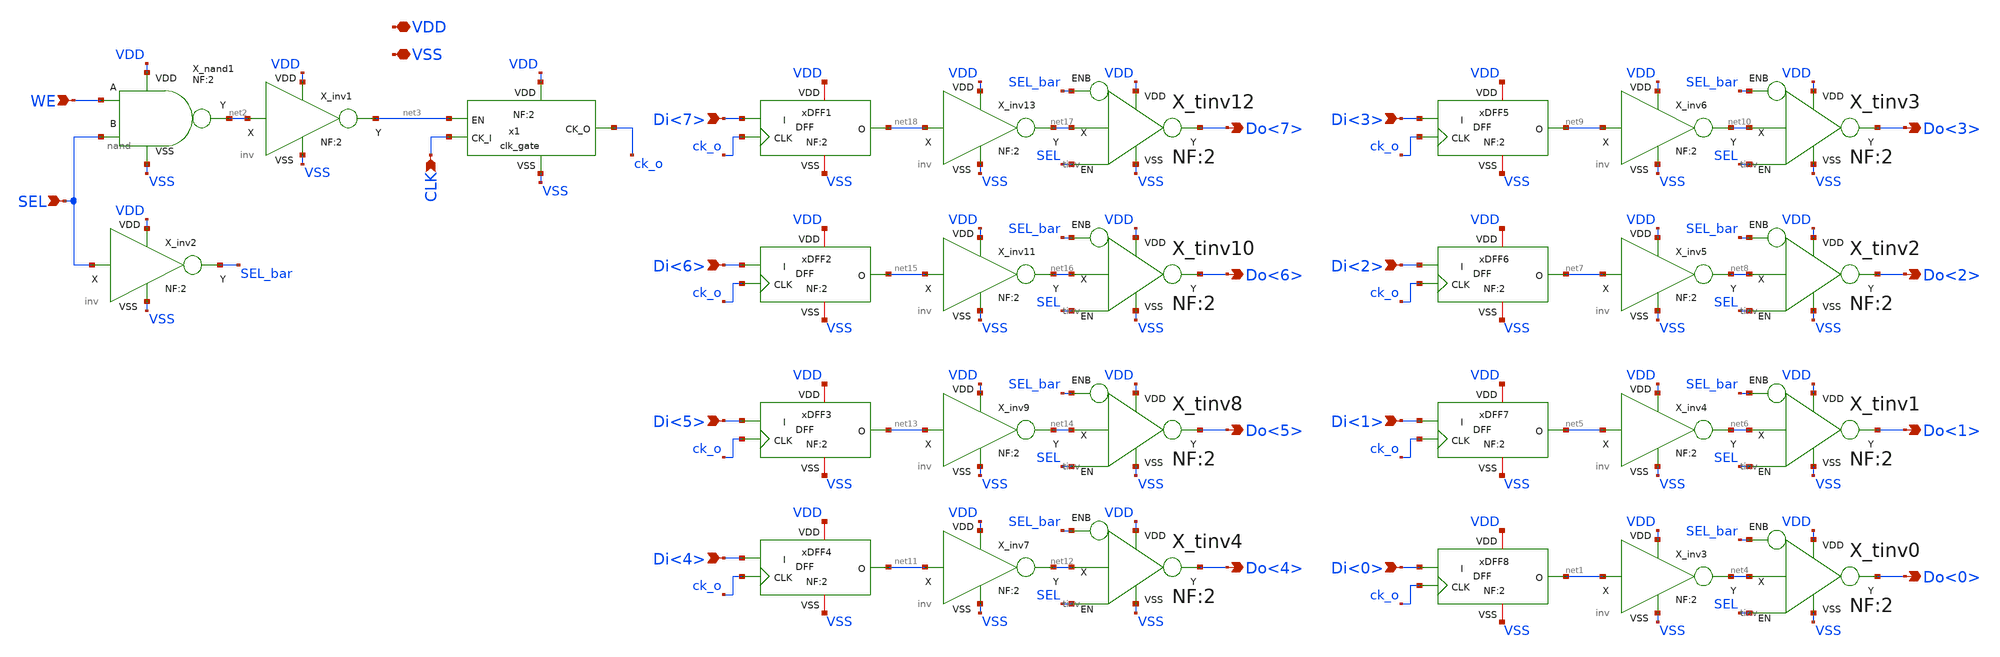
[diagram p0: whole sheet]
** sch_path: xschem_lib/sylee21/byte_dff.sch
**.subckt byte_dff Di<7> Do<6> Di<6> Do<5> Di<5> Di<4> Do<3> Di<3> Do<2> Di<2> Do<1> Di<1> Do<0>
*+ Di<0> WE SEL CLK VDD VSS Do<7> Do<4>
*.ipin Di<7>
*.opin Do<6>
*.ipin Di<6>
*.opin Do<5>
*.ipin Di<5>
*.ipin Di<4>
*.opin Do<3>
*.ipin Di<3>
*.opin Do<2>
*.ipin Di<2>
*.opin Do<1>
*.ipin Di<1>
*.opin Do<0>
*.ipin Di<0>
*.ipin WE
*.ipin SEL
*.ipin CLK
*.iopin VDD
*.iopin VSS
*.opin Do<7>
*.opin Do<4>
X_nand1 SEL WE net2 VDD VSS nand NF=2
X_inv2 SEL VDD VSS SEL_bar inv NF=2
x1 VDD net3 ck_o CLK VSS clk_gate NF=2
xDFF1 VDD VSS Di<7> net18 ck_o DFF NF=2
X_inv1 net2 VDD VSS net3 inv NF=2
X_tinv0 net4 SEL SEL_bar VDD VSS Do<0> tinv NF=2
xDFF2 VDD VSS Di<6> net15 ck_o DFF NF=2
xDFF3 VDD VSS Di<5> net13 ck_o DFF NF=2
xDFF4 VDD VSS Di<4> net11 ck_o DFF NF=2
xDFF5 VDD VSS Di<3> net9 ck_o DFF NF=2
xDFF6 VDD VSS Di<2> net7 ck_o DFF NF=2
xDFF7 VDD VSS Di<1> net5 ck_o DFF NF=2
xDFF8 VDD VSS Di<0> net1 ck_o DFF NF=2
X_inv3 net1 VDD VSS net4 inv NF=2
X_tinv1 net6 SEL SEL_bar VDD VSS Do<1> tinv NF=2
X_inv4 net5 VDD VSS net6 inv NF=2
X_tinv2 net8 SEL SEL_bar VDD VSS Do<2> tinv NF=2
X_inv5 net7 VDD VSS net8 inv NF=2
X_tinv3 net10 SEL SEL_bar VDD VSS Do<3> tinv NF=2
X_inv6 net9 VDD VSS net10 inv NF=2
X_tinv4 net12 SEL SEL_bar VDD VSS Do<4> tinv NF=2
X_inv7 net11 VDD VSS net12 inv NF=2
X_tinv8 net14 SEL SEL_bar VDD VSS Do<5> tinv NF=2
X_inv9 net13 VDD VSS net14 inv NF=2
X_tinv10 net16 SEL SEL_bar VDD VSS Do<6> tinv NF=2
X_inv11 net15 VDD VSS net16 inv NF=2
X_tinv12 net17 SEL SEL_bar VDD VSS Do<7> tinv NF=2
X_inv13 net18 VDD VSS net17 inv NF=2
**.ends
.end
